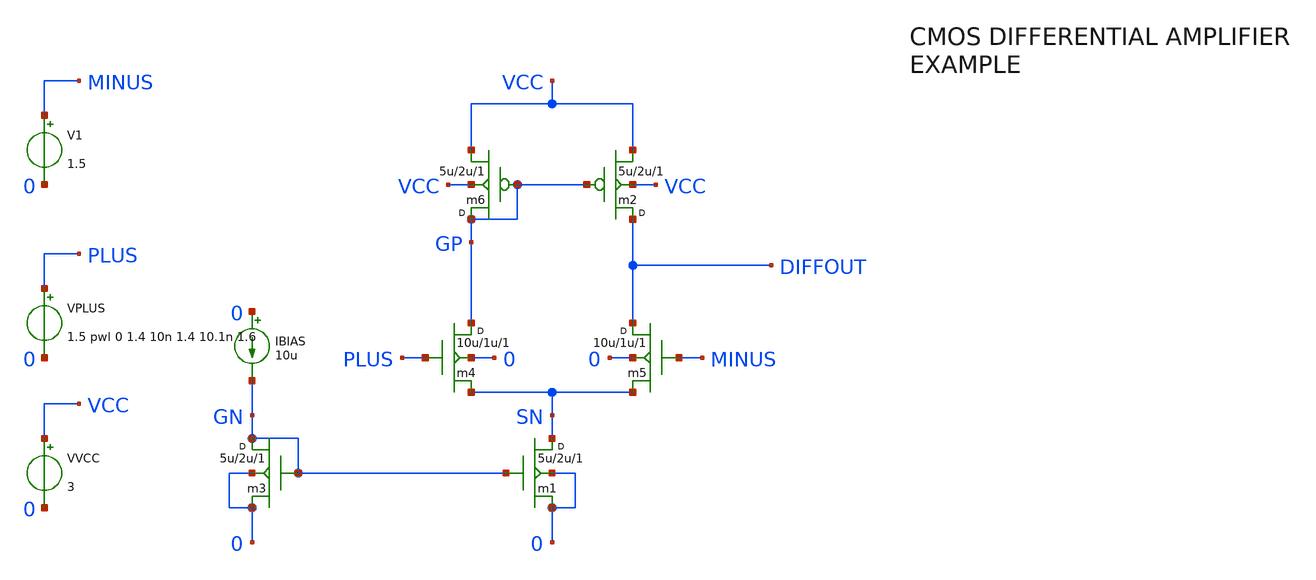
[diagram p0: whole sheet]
** sch_path: xschem_library/examples/cmos_example.sch
**.subckt cmos_example
m1 SN GN 0 0 cmosn w=5u l=2u m=1
m2 DIFFOUT GP VCC VCC cmosp w=5u l=2u m=1
VVCC VCC 0 3
m3 GN GN 0 0 cmosn w=5u l=2u m=1
IBIAS 0 GN 10u
m4 GP PLUS SN 0 cmosn w=10u l=1u m=1
m5 DIFFOUT MINUS SN 0 cmosn w=10u l=1u m=1
m6 GP GP VCC VCC cmosp w=5u l=2u m=1
VPLUS PLUS 0 1.5 pwl 0 1.4 10n 1.4 10.1n 1.6
V1 MINUS 0 1.5
**** begin user architecture code


** ngspice
* .temp 30

** xyce
.step temp list 30

** ngspice
* .save all

** models are generally not free: you must download
** SPICE models for active devices and put them  into the below
** referenced file in netlist/simulation directory.
.include "models_cmos_example.txt"

.tran 0.02n 20n

** ngspice
* .save all

** xyce, not needed if -r given om cmdline
* .print tran format=raw v(diffout) v(plus) v(minus)


**** end user architecture code
**.ends
.end
